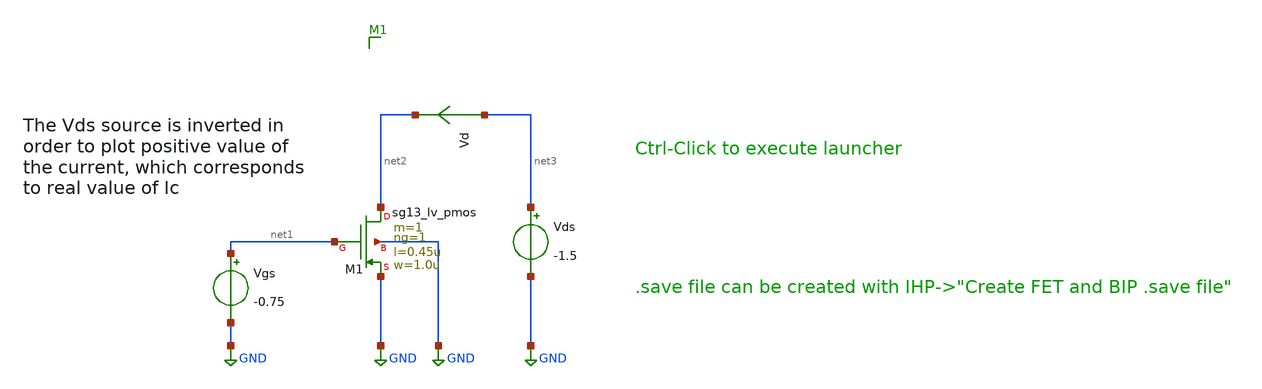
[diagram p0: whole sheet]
** sch_path: ihp-sg13g2/xschem_libs/sg13g2_tests_ase/dc_lv_pmos/schematic/dc_lv_pmos.sch
* Copyright 2023 IHP PDK Authors
**.subckt dc_lv_pmos
Vgs net1 GND -0.75
Vds net3 GND -1.5
XM1 net2 net1 GND GND sg13_lv_pmos w=1.0u l=0.45u ng=1 m=1 mm_ok=1
Vd net3 net2 0
.save i(vd)
**.ends
.GLOBAL GND
.end
